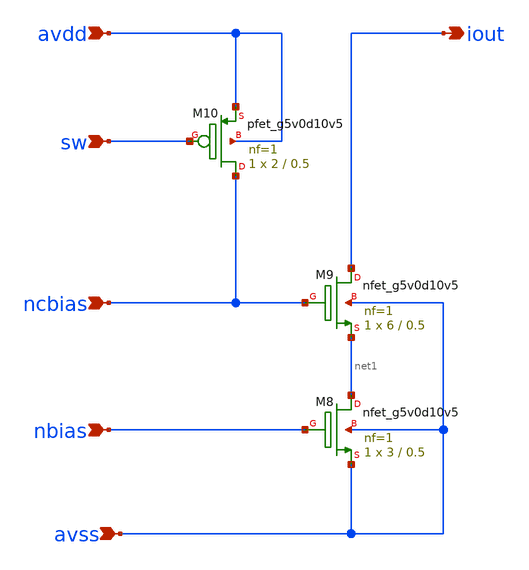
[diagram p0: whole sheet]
** sch_path: xschem/ncell8s.sch
**.subckt ncell8s sw ncbias nbias avss avdd iout
*.ipin sw
*.ipin ncbias
*.ipin nbias
*.ipin avss
*.ipin avdd
*.opin iout
XM8 net1 nbias avss avss sky130_fd_pr__nfet_g5v0d10v5 L=0.5 W=3 nf=1 ad='int((nf+1)/2) * W/nf * 0.29'
+ as='int((nf+2)/2) * W/nf * 0.29' pd='2*int((nf+1)/2) * (W/nf + 0.29)' ps='2*int((nf+2)/2) * (W/nf + 0.29)'
+ nrd='0.29 / W' nrs='0.29 / W' sa=0 sb=0 sd=0 mult=1 m=1
XM9 iout ncbias net1 avss sky130_fd_pr__nfet_g5v0d10v5 L=0.5 W=6 nf=1 ad='int((nf+1)/2) * W/nf * 0.29'
+ as='int((nf+2)/2) * W/nf * 0.29' pd='2*int((nf+1)/2) * (W/nf + 0.29)' ps='2*int((nf+2)/2) * (W/nf + 0.29)'
+ nrd='0.29 / W' nrs='0.29 / W' sa=0 sb=0 sd=0 mult=1 m=1
XM10 ncbias sw avdd avdd sky130_fd_pr__pfet_g5v0d10v5 L=0.5 W=2 nf=1 ad='int((nf+1)/2) * W/nf * 0.29'
+ as='int((nf+2)/2) * W/nf * 0.29' pd='2*int((nf+1)/2) * (W/nf + 0.29)' ps='2*int((nf+2)/2) * (W/nf + 0.29)'
+ nrd='0.29 / W' nrs='0.29 / W' sa=0 sb=0 sd=0 mult=1 m=1
**.ends
.end
